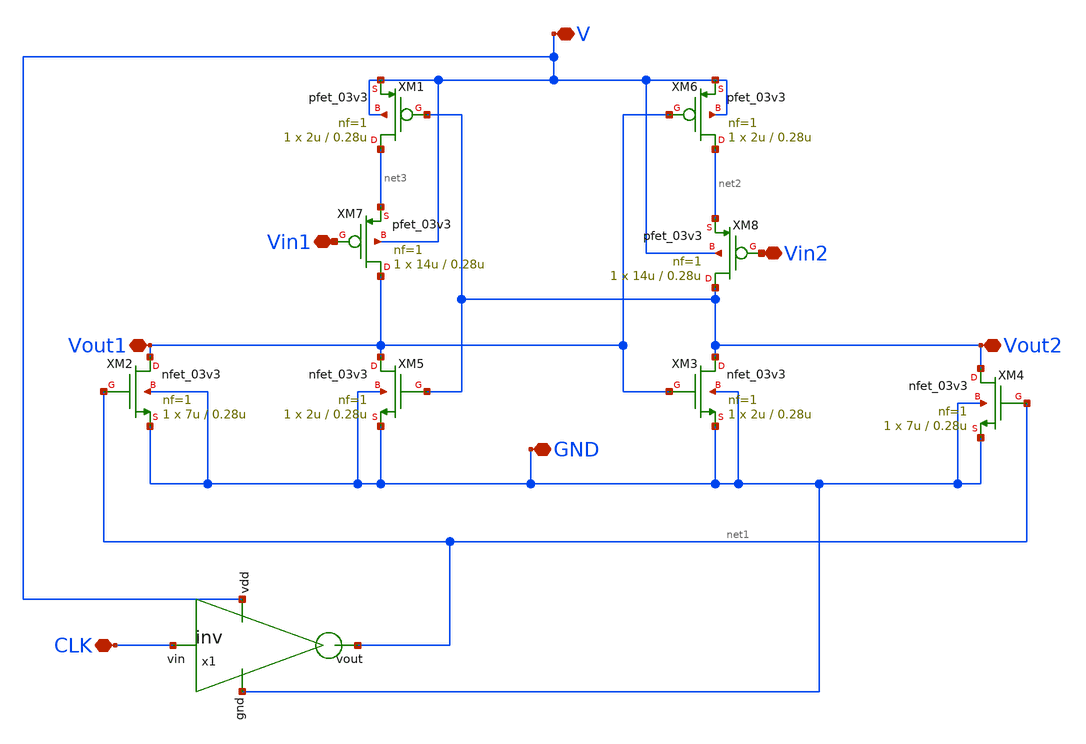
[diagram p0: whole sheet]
** sch_path: Simbolos/strongarm.sch
**.subckt strongarm V Vout1 Vin1 Vin2 Vout2 CLK GND
*.iopin V
*.iopin Vout1
*.iopin Vin1
*.iopin Vin2
*.iopin Vout2
*.iopin CLK
*.iopin GND
XM1 net3 Vout2 V V pfet_03v3 L=0.28u W=2u nf=1 ad='int((nf+1)/2) * W/nf * 0.18u' as='int((nf+2)/2) * W/nf * 0.18u'
+ pd='2*int((nf+1)/2) * (W/nf + 0.18u)' ps='2*int((nf+2)/2) * (W/nf + 0.18u)' nrd='0.18u / W' nrs='0.18u / W'
+ sa=0 sb=0 sd=0 m=1
XM2 Vout1 net1 GND GND nfet_03v3 L=0.28u W=7u nf=1 ad='int((nf+1)/2) * W/nf * 0.18u' as='int((nf+2)/2) * W/nf * 0.18u'
+ pd='2*int((nf+1)/2) * (W/nf + 0.18u)' ps='2*int((nf+2)/2) * (W/nf + 0.18u)' nrd='0.18u / W' nrs='0.18u / W'
+ sa=0 sb=0 sd=0 m=1
XM3 Vout2 Vout1 GND GND nfet_03v3 L=0.28u W=2u nf=1 ad='int((nf+1)/2) * W/nf * 0.18u' as='int((nf+2)/2) * W/nf * 0.18u'
+ pd='2*int((nf+1)/2) * (W/nf + 0.18u)' ps='2*int((nf+2)/2) * (W/nf + 0.18u)' nrd='0.18u / W' nrs='0.18u / W'
+ sa=0 sb=0 sd=0 m=1
XM4 Vout2 net1 GND GND nfet_03v3 L=0.28u W=7u nf=1 ad='int((nf+1)/2) * W/nf * 0.18u' as='int((nf+2)/2) * W/nf * 0.18u'
+ pd='2*int((nf+1)/2) * (W/nf + 0.18u)' ps='2*int((nf+2)/2) * (W/nf + 0.18u)' nrd='0.18u / W' nrs='0.18u / W'
+ sa=0 sb=0 sd=0 m=1
XM5 Vout1 Vout2 GND GND nfet_03v3 L=0.28u W=2u nf=1 ad='int((nf+1)/2) * W/nf * 0.18u' as='int((nf+2)/2) * W/nf * 0.18u'
+ pd='2*int((nf+1)/2) * (W/nf + 0.18u)' ps='2*int((nf+2)/2) * (W/nf + 0.18u)' nrd='0.18u / W' nrs='0.18u / W'
+ sa=0 sb=0 sd=0 m=1
XM6 net2 Vout1 V V pfet_03v3 L=0.28u W=2u nf=1 ad='int((nf+1)/2) * W/nf * 0.18u' as='int((nf+2)/2) * W/nf * 0.18u'
+ pd='2*int((nf+1)/2) * (W/nf + 0.18u)' ps='2*int((nf+2)/2) * (W/nf + 0.18u)' nrd='0.18u / W' nrs='0.18u / W'
+ sa=0 sb=0 sd=0 m=1
XM7 Vout1 Vin1 net3 V pfet_03v3 L=0.28u W=14u nf=1 ad='int((nf+1)/2) * W/nf * 0.18u' as='int((nf+2)/2) * W/nf * 0.18u'
+ pd='2*int((nf+1)/2) * (W/nf + 0.18u)' ps='2*int((nf+2)/2) * (W/nf + 0.18u)' nrd='0.18u / W' nrs='0.18u / W'
+ sa=0 sb=0 sd=0 m=1
XM8 Vout2 Vin2 net2 V pfet_03v3 L=0.28u W=14u nf=1 ad='int((nf+1)/2) * W/nf * 0.18u' as='int((nf+2)/2) * W/nf * 0.18u'
+ pd='2*int((nf+1)/2) * (W/nf + 0.18u)' ps='2*int((nf+2)/2) * (W/nf + 0.18u)' nrd='0.18u / W' nrs='0.18u / W'
+ sa=0 sb=0 sd=0 m=1
x1 V GND net1 CLK inv cl=0.28u wp=0.44u wn=0.22u
**** begin user architecture code

.include /foss/pdks/gf180mcuC/libs.tech/ngspice/design.ngspice
.lib /foss/pdks/gf180mcuC/libs.tech/ngspice/sm141064.ngspice typical

**** end user architecture code
**.ends

* expanding   symbol:  SAR_ADC/SAR_ADC_gf180/xschem/spice/inv.sym # of pins=4
** sym_path: SAR_ADC/SAR_ADC_gf180/xschem/spice/inv.sym
** sch_path: SAR_ADC/SAR_ADC_gf180/xschem/spice/inv.sch
.subckt inv vdd gnd vout vin  cl=0.28u wp=0.44u wn=0.22u
*.ipin gnd
*.ipin vdd
*.ipin vin
*.opin vout
XM1 gnd vin vout gnd nfet_03v3 L=0.28u W=4u nf=1 ad='int((nf+1)/2) * W/nf * 0.18u' as='int((nf+2)/2) * W/nf * 0.18u'
+ pd='2*int((nf+1)/2) * (W/nf + 0.18u)' ps='2*int((nf+2)/2) * (W/nf + 0.18u)' nrd='0.18u / W' nrs='0.18u / W'
+ sa=0 sb=0 sd=0 m=1
XM2 vdd vin vout vdd pfet_03v3 L=0.28u W=4u nf=1 ad='int((nf+1)/2) * W/nf * 0.18u' as='int((nf+2)/2) * W/nf * 0.18u'
+ pd='2*int((nf+1)/2) * (W/nf + 0.18u)' ps='2*int((nf+2)/2) * (W/nf + 0.18u)' nrd='0.18u / W' nrs='0.18u / W'
+ sa=0 sb=0 sd=0 m=1
.ends

.end
